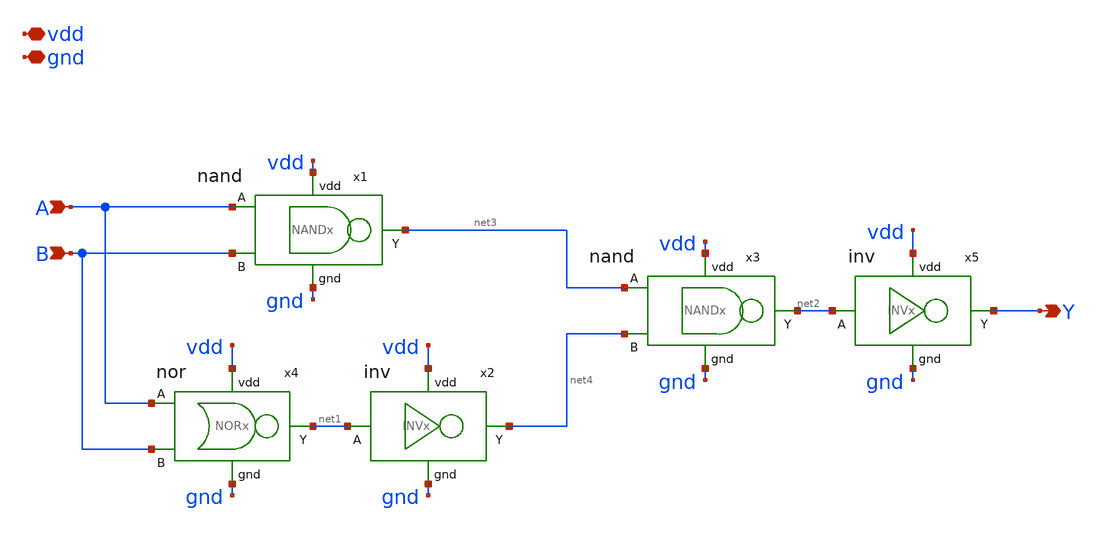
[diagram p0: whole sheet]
** sch_path: lab7/sch/made/XORx.sch
**.subckt XORx A B Y vdd gnd
*.ipin A
*.ipin B
*.opin Y
*.iopin vdd
*.iopin gnd
x4 vdd A net1 B gnd NORx
x2 vdd net1 net4 gnd INVx
x3 vdd net3 net2 net4 gnd NANDx
x5 vdd net2 Y gnd INVx
x1 vdd A net3 B gnd NANDx
**.ends

* expanding   symbol:  /home/dayesong/ETRI050_DesignKit/lab7/sch/NORx.sym # of pins=5
** sym_path: lab7/sch/made/NORx.sym
** sch_path: lab7/sch/made/NORx.sch
.subckt NORx vdd A Y B gnd
*.ipin A
*.ipin B
*.opin Y
*.iopin vdd
*.iopin gnd
M1 net1 A vdd vdd pfet w=12u l=0.6u m=1
M2 Y B net1 vdd pfet w=12u l=0.6u m=1
M3 Y B gnd gnd nfet w=3u l=0.6u m=1
M4 Y A gnd gnd nfet w=3u l=0.6u m=1
.ends


* expanding   symbol:  /home/dayesong/ETRI050_DesignKit/lab7/sch/INVx.sym # of pins=4
** sym_path: lab7/sch/made/INVx.sym
** sch_path: lab7/sch/made/INVx.sch
.subckt INVx vdd A Y gnd
*.ipin A
*.opin Y
*.iopin vdd
*.iopin gnd
M1 Y A vdd vdd pfet w=6u l=0.6u m=1
M2 Y A gnd gnd nfet w=3u l=0.6u m=1
.ends


* expanding   symbol:  /home/dayesong/ETRI050_DesignKit/lab7/sch/NANDx.sym # of pins=5
** sym_path: lab7/sch/made/NANDx.sym
** sch_path: lab7/sch/made/NANDx.sch
.subckt NANDx vdd A Y B gnd
*.ipin A
*.ipin B
*.opin Y
*.iopin vdd
*.iopin gnd
M3 Y B net1 gnd nfet w=6u l=0.6u m=1
M4 Y B vdd vdd pfet w=6u l=0.6u m=1
M2 Y A vdd vdd pfet w=6u l=0.6u m=1
M1 net1 A gnd gnd nfet w=6u l=0.6u m=1
.ends

.end
